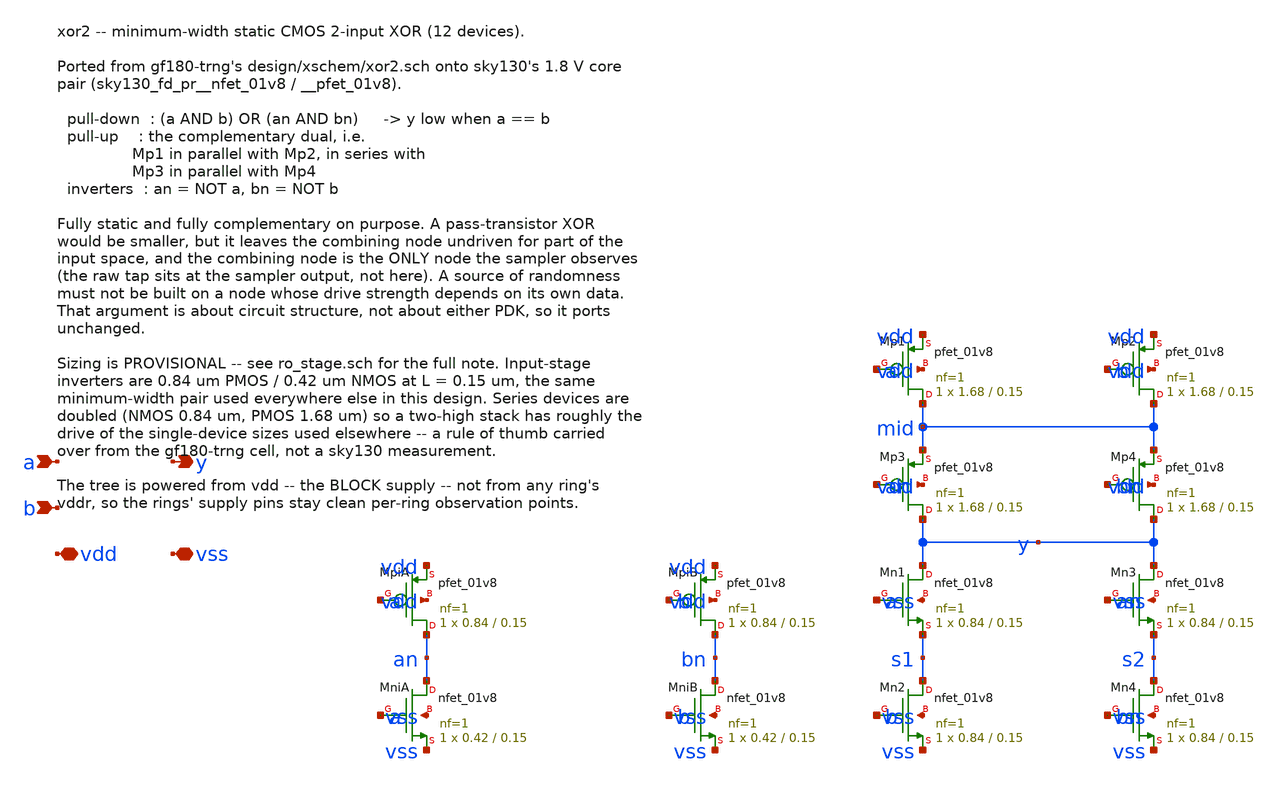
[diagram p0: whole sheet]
** sch_path: design/xschem/xor2.sch
**.subckt xor2 a b y vdd vss
*.ipin a
*.ipin b
*.opin y
*.iopin vdd
*.iopin vss
XMpiA an a vdd vdd sky130_fd_pr__pfet_01v8 L=0.15 W=0.84 nf=1 ad='int((nf+1)/2) * W/nf * 0.29' as='int((nf+2)/2) * W/nf * 0.29'
+ pd='2*int((nf+1)/2) * (W/nf + 0.29)' ps='2*int((nf+2)/2) * (W/nf + 0.29)' nrd='0.29 / W' nrs='0.29 / W'
+ sa=0 sb=0 sd=0 mult=1 m=1
XMniA an a vss vss sky130_fd_pr__nfet_01v8 L=0.15 W=0.42 nf=1 ad='int((1 + 1)/2) * 0.42 / 1 * 0.29' as='int((1 + 2)/2) * 0.42 / 1 * 0.29'
+ pd='2*int((1 + 1)/2) * (0.42 / 1 + 0.29)' ps='2*int((1 + 2)/2) * (0.42 / 1 + 0.29)' nrd='0.29 / 0.42 '
+ nrs='0.29 / 0.42 ' sa=0 sb=0 sd=0 mult=1 m=1
XMpiB bn b vdd vdd sky130_fd_pr__pfet_01v8 L=0.15 W=0.84 nf=1 ad='int((nf+1)/2) * W/nf * 0.29' as='int((nf+2)/2) * W/nf * 0.29'
+ pd='2*int((nf+1)/2) * (W/nf + 0.29)' ps='2*int((nf+2)/2) * (W/nf + 0.29)' nrd='0.29 / W' nrs='0.29 / W'
+ sa=0 sb=0 sd=0 mult=1 m=1
XMniB bn b vss vss sky130_fd_pr__nfet_01v8 L=0.15 W=0.42 nf=1 ad='int((1 + 1)/2) * 0.42 / 1 * 0.29' as='int((1 + 2)/2) * 0.42 / 1 * 0.29'
+ pd='2*int((1 + 1)/2) * (0.42 / 1 + 0.29)' ps='2*int((1 + 2)/2) * (0.42 / 1 + 0.29)' nrd='0.29 / 0.42 '
+ nrs='0.29 / 0.42 ' sa=0 sb=0 sd=0 mult=1 m=1
XMp1 mid a vdd vdd sky130_fd_pr__pfet_01v8 L=0.15 W=1.68 nf=1 ad='int((nf+1)/2) * W/nf * 0.29' as='int((nf+2)/2) * W/nf * 0.29'
+ pd='2*int((nf+1)/2) * (W/nf + 0.29)' ps='2*int((nf+2)/2) * (W/nf + 0.29)' nrd='0.29 / W' nrs='0.29 / W'
+ sa=0 sb=0 sd=0 mult=1 m=1
XMp2 mid b vdd vdd sky130_fd_pr__pfet_01v8 L=0.15 W=1.68 nf=1 ad='int((nf+1)/2) * W/nf * 0.29' as='int((nf+2)/2) * W/nf * 0.29'
+ pd='2*int((nf+1)/2) * (W/nf + 0.29)' ps='2*int((nf+2)/2) * (W/nf + 0.29)' nrd='0.29 / W' nrs='0.29 / W'
+ sa=0 sb=0 sd=0 mult=1 m=1
XMp3 y an mid vdd sky130_fd_pr__pfet_01v8 L=0.15 W=1.68 nf=1 ad='int((nf+1)/2) * W/nf * 0.29' as='int((nf+2)/2) * W/nf * 0.29'
+ pd='2*int((nf+1)/2) * (W/nf + 0.29)' ps='2*int((nf+2)/2) * (W/nf + 0.29)' nrd='0.29 / W' nrs='0.29 / W'
+ sa=0 sb=0 sd=0 mult=1 m=1
XMp4 y bn mid vdd sky130_fd_pr__pfet_01v8 L=0.15 W=1.68 nf=1 ad='int((nf+1)/2) * W/nf * 0.29' as='int((nf+2)/2) * W/nf * 0.29'
+ pd='2*int((nf+1)/2) * (W/nf + 0.29)' ps='2*int((nf+2)/2) * (W/nf + 0.29)' nrd='0.29 / W' nrs='0.29 / W'
+ sa=0 sb=0 sd=0 mult=1 m=1
XMn1 y a s1 vss sky130_fd_pr__nfet_01v8 L=0.15 W=0.84 nf=1 ad='int((1 + 1)/2) * 0.84 / 1 * 0.29' as='int((1 + 2)/2) * 0.84 / 1 * 0.29'
+ pd='2*int((1 + 1)/2) * (0.84 / 1 + 0.29)' ps='2*int((1 + 2)/2) * (0.84 / 1 + 0.29)' nrd='0.29 / 0.84 '
+ nrs='0.29 / 0.84 ' sa=0 sb=0 sd=0 mult=1 m=1
XMn2 s1 b vss vss sky130_fd_pr__nfet_01v8 L=0.15 W=0.84 nf=1 ad='int((1 + 1)/2) * 0.84 / 1 * 0.29' as='int((1 + 2)/2) * 0.84 / 1 * 0.29'
+ pd='2*int((1 + 1)/2) * (0.84 / 1 + 0.29)' ps='2*int((1 + 2)/2) * (0.84 / 1 + 0.29)' nrd='0.29 / 0.84 '
+ nrs='0.29 / 0.84 ' sa=0 sb=0 sd=0 mult=1 m=1
XMn3 y an s2 vss sky130_fd_pr__nfet_01v8 L=0.15 W=0.84 nf=1 ad='int((1 + 1)/2) * 0.84 / 1 * 0.29' as='int((1 + 2)/2) * 0.84 / 1 * 0.29'
+ pd='2*int((1 + 1)/2) * (0.84 / 1 + 0.29)' ps='2*int((1 + 2)/2) * (0.84 / 1 + 0.29)' nrd='0.29 / 0.84 '
+ nrs='0.29 / 0.84 ' sa=0 sb=0 sd=0 mult=1 m=1
XMn4 s2 bn vss vss sky130_fd_pr__nfet_01v8 L=0.15 W=0.84 nf=1 ad='int((1 + 1)/2) * 0.84 / 1 * 0.29' as='int((1 + 2)/2) * 0.84 / 1 * 0.29'
+ pd='2*int((1 + 1)/2) * (0.84 / 1 + 0.29)' ps='2*int((1 + 2)/2) * (0.84 / 1 + 0.29)' nrd='0.29 / 0.84 '
+ nrs='0.29 / 0.84 ' sa=0 sb=0 sd=0 mult=1 m=1
**.ends
.end
